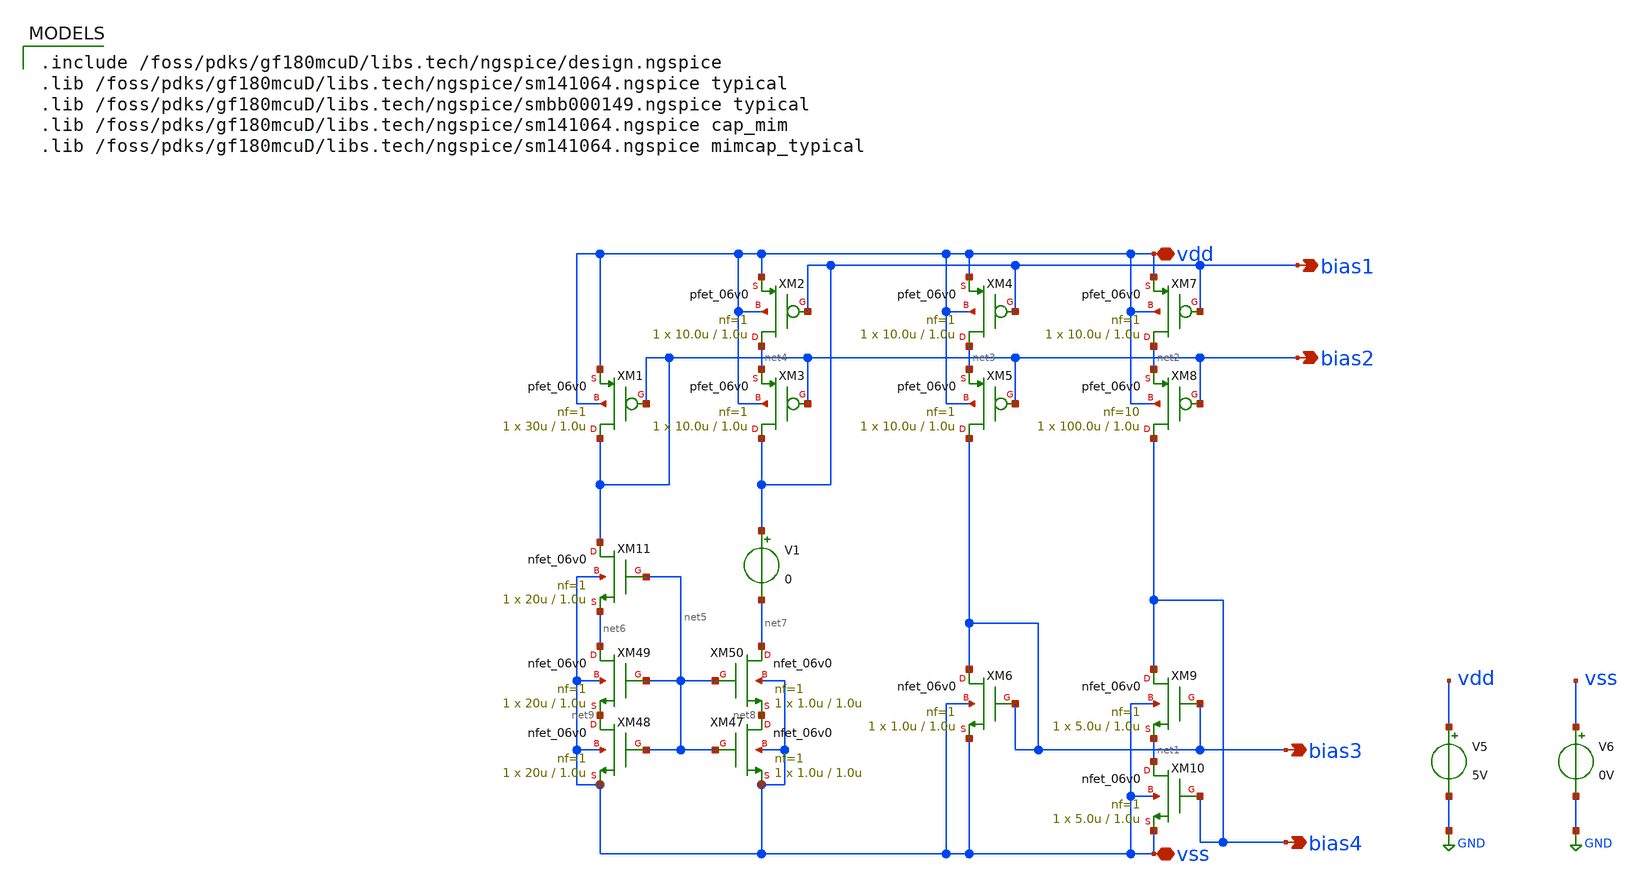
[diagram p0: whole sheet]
** sch_path: activities/opamp2Enzo/biasTB2_Enzo.sch
**.subckt biasTB2_Enzo bias1 bias2 bias3 bias4 vdd vss
*.opin bias1
*.opin bias2
*.opin bias3
*.opin bias4
*.iopin vdd
*.iopin vss
V5 vdd GND 5V
V6 vss GND 0V
XM4 net3 bias1 vdd vdd pfet_06v0 L=1.0u W=10.0u nf=1 ad='int((nf+1)/2) * W/nf * 0.18u' as='int((nf+2)/2) * W/nf * 0.18u'
+ pd='2*int((nf+1)/2) * (W/nf + 0.18u)' ps='2*int((nf+2)/2) * (W/nf + 0.18u)' nrd='0.18u / W' nrs='0.18u / W'
+ sa=0 sb=0 sd=0 m=1
XM5 bias3 bias2 net3 vdd pfet_06v0 L=1.0u W=10.0u nf=1 ad='int((nf+1)/2) * W/nf * 0.18u' as='int((nf+2)/2) * W/nf * 0.18u'
+ pd='2*int((nf+1)/2) * (W/nf + 0.18u)' ps='2*int((nf+2)/2) * (W/nf + 0.18u)' nrd='0.18u / W' nrs='0.18u / W'
+ sa=0 sb=0 sd=0 m=1
XM6 bias3 bias3 vss vss nfet_06v0 L=1.0u W=1.0u nf=1 ad='int((nf+1)/2) * W/nf * 0.18u' as='int((nf+2)/2) * W/nf * 0.18u'
+ pd='2*int((nf+1)/2) * (W/nf + 0.18u)' ps='2*int((nf+2)/2) * (W/nf + 0.18u)' nrd='0.18u / W' nrs='0.18u / W'
+ sa=0 sb=0 sd=0 m=1
XM7 net2 bias1 vdd vdd pfet_06v0 L=1.0u W=10.0u nf=1 ad='int((nf+1)/2) * W/nf * 0.18u' as='int((nf+2)/2) * W/nf * 0.18u'
+ pd='2*int((nf+1)/2) * (W/nf + 0.18u)' ps='2*int((nf+2)/2) * (W/nf + 0.18u)' nrd='0.18u / W' nrs='0.18u / W'
+ sa=0 sb=0 sd=0 m=1
XM8 bias4 bias2 net2 vdd pfet_06v0 L=1.0u W=100.0u nf=10 ad='int((nf+1)/2) * W/nf * 0.18u' as='int((nf+2)/2) * W/nf * 0.18u'
+ pd='2*int((nf+1)/2) * (W/nf + 0.18u)' ps='2*int((nf+2)/2) * (W/nf + 0.18u)' nrd='0.18u / W' nrs='0.18u / W'
+ sa=0 sb=0 sd=0 m=1
XM9 bias4 bias3 net1 vss nfet_06v0 L=1.0u W=5.0u nf=1 ad='int((nf+1)/2) * W/nf * 0.18u' as='int((nf+2)/2) * W/nf * 0.18u'
+ pd='2*int((nf+1)/2) * (W/nf + 0.18u)' ps='2*int((nf+2)/2) * (W/nf + 0.18u)' nrd='0.18u / W' nrs='0.18u / W'
+ sa=0 sb=0 sd=0 m=1
XM10 net1 bias4 vss vss nfet_06v0 L=1.0u W=5.0u nf=1 ad='int((nf+1)/2) * W/nf * 0.18u' as='int((nf+2)/2) * W/nf * 0.18u'
+ pd='2*int((nf+1)/2) * (W/nf + 0.18u)' ps='2*int((nf+2)/2) * (W/nf + 0.18u)' nrd='0.18u / W' nrs='0.18u / W'
+ sa=0 sb=0 sd=0 m=1
XM1 bias2 bias2 vdd vdd pfet_06v0 L=1.0u W=30u nf=1 ad='int((nf+1)/2) * W/nf * 0.18u' as='int((nf+2)/2) * W/nf * 0.18u'
+ pd='2*int((nf+1)/2) * (W/nf + 0.18u)' ps='2*int((nf+2)/2) * (W/nf + 0.18u)' nrd='0.18u / W' nrs='0.18u / W'
+ sa=0 sb=0 sd=0 m=1
XM2 net4 bias1 vdd vdd pfet_06v0 L=1.0u W=10.0u nf=1 ad='int((nf+1)/2) * W/nf * 0.18u' as='int((nf+2)/2) * W/nf * 0.18u'
+ pd='2*int((nf+1)/2) * (W/nf + 0.18u)' ps='2*int((nf+2)/2) * (W/nf + 0.18u)' nrd='0.18u / W' nrs='0.18u / W'
+ sa=0 sb=0 sd=0 m=1
XM3 bias1 bias2 net4 vdd pfet_06v0 L=1.0u W=10.0u nf=1 ad='int((nf+1)/2) * W/nf * 0.18u' as='int((nf+2)/2) * W/nf * 0.18u'
+ pd='2*int((nf+1)/2) * (W/nf + 0.18u)' ps='2*int((nf+2)/2) * (W/nf + 0.18u)' nrd='0.18u / W' nrs='0.18u / W'
+ sa=0 sb=0 sd=0 m=1
XM47 net8 net5 vss vss nfet_06v0 L=1.0u W=1.0u nf=1 ad='int((nf+1)/2) * W/nf * 0.18u' as='int((nf+2)/2) * W/nf * 0.18u'
+ pd='2*int((nf+1)/2) * (W/nf + 0.18u)' ps='2*int((nf+2)/2) * (W/nf + 0.18u)' nrd='0.18u / W' nrs='0.18u / W'
+ sa=0 sb=0 sd=0 m=1
XM48 net9 net5 vss vss nfet_06v0 L=1.0u W=20u nf=1 ad='int((nf+1)/2) * W/nf * 0.18u' as='int((nf+2)/2) * W/nf * 0.18u'
+ pd='2*int((nf+1)/2) * (W/nf + 0.18u)' ps='2*int((nf+2)/2) * (W/nf + 0.18u)' nrd='0.18u / W' nrs='0.18u / W'
+ sa=0 sb=0 sd=0 m=1
XM49 net6 net5 net9 vss nfet_06v0 L=1.0u W=20u nf=1 ad='int((nf+1)/2) * W/nf * 0.18u' as='int((nf+2)/2) * W/nf * 0.18u'
+ pd='2*int((nf+1)/2) * (W/nf + 0.18u)' ps='2*int((nf+2)/2) * (W/nf + 0.18u)' nrd='0.18u / W' nrs='0.18u / W'
+ sa=0 sb=0 sd=0 m=1
XM50 net7 net5 net8 vss nfet_06v0 L=1.0u W=1.0u nf=1 ad='int((nf+1)/2) * W/nf * 0.18u' as='int((nf+2)/2) * W/nf * 0.18u'
+ pd='2*int((nf+1)/2) * (W/nf + 0.18u)' ps='2*int((nf+2)/2) * (W/nf + 0.18u)' nrd='0.18u / W' nrs='0.18u / W'
+ sa=0 sb=0 sd=0 m=1
XM11 bias2 net5 net6 vss nfet_06v0 L=1.0u W=20u nf=1 ad='int((nf+1)/2) * W/nf * 0.18u' as='int((nf+2)/2) * W/nf * 0.18u'
+ pd='2*int((nf+1)/2) * (W/nf + 0.18u)' ps='2*int((nf+2)/2) * (W/nf + 0.18u)' nrd='0.18u / W' nrs='0.18u / W'
+ sa=0 sb=0 sd=0 m=1
V1 bias1 net7 0
**** begin user architecture code

.include /foss/pdks/gf180mcuD/libs.tech/ngspice/design.ngspice
.lib /foss/pdks/gf180mcuD/libs.tech/ngspice/sm141064.ngspice typical
.lib /foss/pdks/gf180mcuD/libs.tech/ngspice/smbb000149.ngspice typical
.lib /foss/pdks/gf180mcuD/libs.tech/ngspice/sm141064.ngspice cap_mim
.lib /foss/pdks/gf180mcuD/libs.tech/ngspice/sm141064.ngspice mimcap_typical




.control
  op
  let b1 = v(bias1)
  let b2 = v(bias2)
  let b3 = v(bias3)
  let b4 = v(bias4)
  echo "$&b1 $&b2 $&b3 $&b4" >>
+ /foss/designs/sscs-2026-zotnetic/activities/opamp2Enzo/Sim_results/biasTB2_results.txt
.endc

**** end user architecture code
**.ends
.GLOBAL GND
.end
